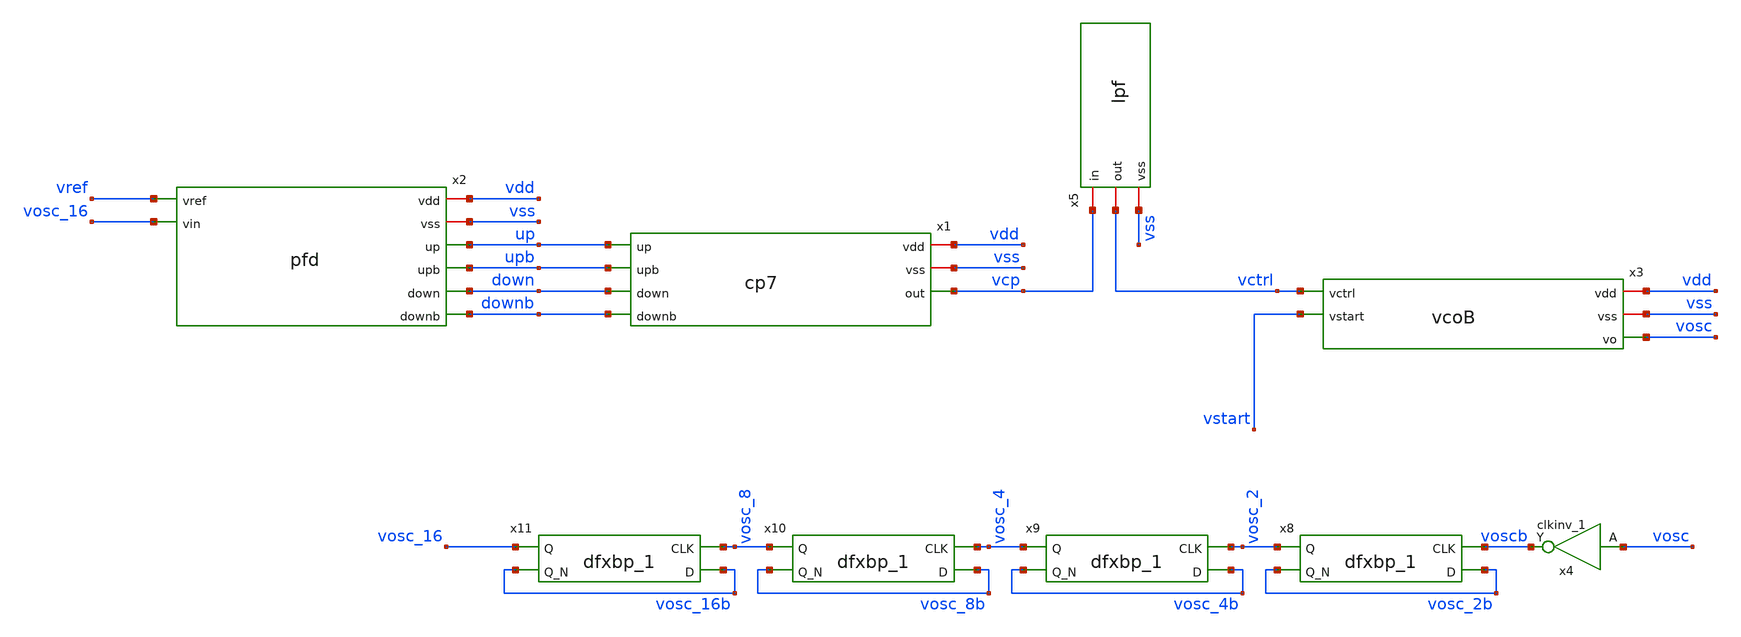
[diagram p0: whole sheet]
** sch_path: custom_gds/tt_um_mickey_pll/xschem/pll.sch
* custom_gds/tt_um_mickey_pll/xschem/inv_0p25.sym:
* Copyright 2022 Stefan Frederik Schippers
* Licensed under the Apache License, Version 2.0 (the "License");
.lib $::SKYWATER_MODELS/sky130.lib.spice tt
.include $::SKYWATER_STDCELLS/sky130_fd_sc_hd.spice

**.subckt pll
x1 vdd vss upb up vcp down downb cp7
x2 vdd vss vref up upb down vosc_16 downb pfd
x3 vdd vss vctrl vosc vstart vcoB
x8 voscb vosc_2b vss vss vdd vdd vosc_2 vosc_2b sky130_fd_sc_hd__dfxbp_1
x9 vosc_2 vosc_4b vss vss vdd vdd vosc_4 vosc_4b sky130_fd_sc_hd__dfxbp_1
x10 vosc_4 vosc_8b vss vss vdd vdd vosc_8 vosc_8b sky130_fd_sc_hd__dfxbp_1
x11 vosc_8 vosc_16b vss vss vdd vdd vosc_16 vosc_16b sky130_fd_sc_hd__dfxbp_1
x4 vosc vss vss vdd vdd voscb sky130_fd_sc_hd__clkinv_1
x5 vcp vctrl vss lpf
**** begin user architecture code



.param VCC=1.8
.options savecurrents
vvss vss 0 dc 0
vvdd vdd 0 dc VCC
**** vvctrl vctrl 0 dc 0.9
****vvctrl vctrl 0 PWL(0 0.9 100p 0.9 1000n 1.5)
vvstart vstart 0 PWL(0 1.8 100p 1.8 200p 0.0) dc 0
****vvstarve2 vstarve2 0 dc 1.8
vvref vref 0 PULSE(0.0 1.8 0n 1n 1n 80n 160n) dc 0

.ic v(vctrl)=0.8 v(vref)=0 v(vosc)=0

**** .ic v(vo_0)=1.8 v(vo_12)=0.0

**** interactive sim
.control
  remzerovec
  save all
  tran 100p 50000n
  remzerovec
  write untitled.raw
.endc



**** end user architecture code
**.ends

* expanding   symbol:  cp7.sym # of pins=7
** sym_path: custom_gds/tt_um_mickey_pll/xschem/cp7.sym
** sch_path: custom_gds/tt_um_mickey_pll/xschem/cp7.sch
.subckt cp7 vdd vss upb up out down downb
*.ipin upb
*.ipin up
*.ipin down
*.ipin downb
*.opin out
*.iopin vdd
*.iopin vss
XM1 vnb2 vnb3 vss vss sky130_fd_pr__nfet_01v8 L=0.60 W=1.80 nf=1 ad='int((nf+1)/2) * W/nf * 0.29' as='int((nf+2)/2) * W/nf * 0.29'
+ pd='2*int((nf+1)/2) * (W/nf + 0.29)' ps='2*int((nf+2)/2) * (W/nf + 0.29)' nrd='0.29 / W' nrs='0.29 / W'
+ sa=0 sb=0 sd=0 mult=1 m=1
XM2 out vnb vnb2 vss sky130_fd_pr__nfet_01v8 L=0.60 W=1.80 nf=1 ad='int((nf+1)/2) * W/nf * 0.29' as='int((nf+2)/2) * W/nf * 0.29'
+ pd='2*int((nf+1)/2) * (W/nf + 0.29)' ps='2*int((nf+2)/2) * (W/nf + 0.29)' nrd='0.29 / W' nrs='0.29 / W'
+ sa=0 sb=0 sd=0 mult=1 m=1
XM3 vnb3 vnb net1 vss sky130_fd_pr__nfet_01v8 L=0.60 W=1.80 nf=1 ad='int((nf+1)/2) * W/nf * 0.29' as='int((nf+2)/2) * W/nf * 0.29'
+ pd='2*int((nf+1)/2) * (W/nf + 0.29)' ps='2*int((nf+2)/2) * (W/nf + 0.29)' nrd='0.29 / W' nrs='0.29 / W'
+ sa=0 sb=0 sd=0 mult=1 m=1
XM4 net1 vnb3 vss vss sky130_fd_pr__nfet_01v8 L=0.60 W=1.80 nf=1 ad='int((nf+1)/2) * W/nf * 0.29' as='int((nf+2)/2) * W/nf * 0.29'
+ pd='2*int((nf+1)/2) * (W/nf + 0.29)' ps='2*int((nf+2)/2) * (W/nf + 0.29)' nrd='0.29 / W' nrs='0.29 / W'
+ sa=0 sb=0 sd=0 mult=1 m=1
XM5 vpb2 upb vss vss sky130_fd_pr__nfet_01v8 L=0.15 W=0.45 nf=1 ad='int((nf+1)/2) * W/nf * 0.29' as='int((nf+2)/2) * W/nf * 0.29'
+ pd='2*int((nf+1)/2) * (W/nf + 0.29)' ps='2*int((nf+2)/2) * (W/nf + 0.29)' nrd='0.29 / W' nrs='0.29 / W'
+ sa=0 sb=0 sd=0 mult=1 m=1
XM8 out vpb vpb2 vdd sky130_fd_pr__pfet_01v8 L=0.60 W=1.80 nf=1 ad='int((nf+1)/2) * W/nf * 0.29' as='int((nf+2)/2) * W/nf * 0.29'
+ pd='2*int((nf+1)/2) * (W/nf + 0.29)' ps='2*int((nf+2)/2) * (W/nf + 0.29)' nrd='0.29 / W' nrs='0.29 / W'
+ sa=0 sb=0 sd=0 mult=1 m=1
XM6 vpb2 vpb3 vdd vdd sky130_fd_pr__pfet_01v8 L=0.60 W=1.80 nf=1 ad='int((nf+1)/2) * W/nf * 0.29' as='int((nf+2)/2) * W/nf * 0.29'
+ pd='2*int((nf+1)/2) * (W/nf + 0.29)' ps='2*int((nf+2)/2) * (W/nf + 0.29)' nrd='0.29 / W' nrs='0.29 / W'
+ sa=0 sb=0 sd=0 mult=1 m=1
XM7 vpb3 vpb net2 vdd sky130_fd_pr__pfet_01v8 L=0.60 W=1.80 nf=1 ad='int((nf+1)/2) * W/nf * 0.29' as='int((nf+2)/2) * W/nf * 0.29'
+ pd='2*int((nf+1)/2) * (W/nf + 0.29)' ps='2*int((nf+2)/2) * (W/nf + 0.29)' nrd='0.29 / W' nrs='0.29 / W'
+ sa=0 sb=0 sd=0 mult=1 m=1
XM9 net2 vpb3 vdd vdd sky130_fd_pr__pfet_01v8 L=0.60 W=1.80 nf=1 ad='int((nf+1)/2) * W/nf * 0.29' as='int((nf+2)/2) * W/nf * 0.29'
+ pd='2*int((nf+1)/2) * (W/nf + 0.29)' ps='2*int((nf+2)/2) * (W/nf + 0.29)' nrd='0.29 / W' nrs='0.29 / W'
+ sa=0 sb=0 sd=0 mult=1 m=1
XM10 vnb2 down vdd vdd sky130_fd_pr__pfet_01v8 L=0.15 W=0.60 nf=1 ad='int((nf+1)/2) * W/nf * 0.29' as='int((nf+2)/2) * W/nf * 0.29'
+ pd='2*int((nf+1)/2) * (W/nf + 0.29)' ps='2*int((nf+2)/2) * (W/nf + 0.29)' nrd='0.29 / W' nrs='0.29 / W'
+ sa=0 sb=0 sd=0 mult=1 m=1
XM11 vnb vnb vss vss sky130_fd_pr__nfet_01v8 L=0.60 W=0.45 nf=1 ad='int((nf+1)/2) * W/nf * 0.29' as='int((nf+2)/2) * W/nf * 0.29'
+ pd='2*int((nf+1)/2) * (W/nf + 0.29)' ps='2*int((nf+2)/2) * (W/nf + 0.29)' nrd='0.29 / W' nrs='0.29 / W'
+ sa=0 sb=0 sd=0 mult=1 m=1
XM12 vpb vpb vdd vdd sky130_fd_pr__pfet_01v8 L=0.60 W=0.45 nf=1 ad='int((nf+1)/2) * W/nf * 0.29' as='int((nf+2)/2) * W/nf * 0.29'
+ pd='2*int((nf+1)/2) * (W/nf + 0.29)' ps='2*int((nf+2)/2) * (W/nf + 0.29)' nrd='0.29 / W' nrs='0.29 / W'
+ sa=0 sb=0 sd=0 mult=1 m=1
x2 vdd G_vnb G_vpb vss bias
XM13 vnb G_vpb vdd vdd sky130_fd_pr__pfet_01v8 L=0.60 W=1.80 nf=1 ad='int((nf+1)/2) * W/nf * 0.29' as='int((nf+2)/2) * W/nf * 0.29'
+ pd='2*int((nf+1)/2) * (W/nf + 0.29)' ps='2*int((nf+2)/2) * (W/nf + 0.29)' nrd='0.29 / W' nrs='0.29 / W'
+ sa=0 sb=0 sd=0 mult=1 m=1
XM14 vpb G_vnb vss vss sky130_fd_pr__nfet_01v8 L=0.60 W=1.80 nf=1 ad='int((nf+1)/2) * W/nf * 0.29' as='int((nf+2)/2) * W/nf * 0.29'
+ pd='2*int((nf+1)/2) * (W/nf + 0.29)' ps='2*int((nf+2)/2) * (W/nf + 0.29)' nrd='0.29 / W' nrs='0.29 / W'
+ sa=0 sb=0 sd=0 mult=1 m=1
XM15 vpb3 G_vnb vss vss sky130_fd_pr__nfet_01v8 L=0.60 W=1.80 nf=1 ad='int((nf+1)/2) * W/nf * 0.29' as='int((nf+2)/2) * W/nf * 0.29'
+ pd='2*int((nf+1)/2) * (W/nf + 0.29)' ps='2*int((nf+2)/2) * (W/nf + 0.29)' nrd='0.29 / W' nrs='0.29 / W'
+ sa=0 sb=0 sd=0 mult=1 m=1
XM16 vnb3 G_vpb vdd vdd sky130_fd_pr__pfet_01v8 L=0.60 W=1.80 nf=1 ad='int((nf+1)/2) * W/nf * 0.29' as='int((nf+2)/2) * W/nf * 0.29'
+ pd='2*int((nf+1)/2) * (W/nf + 0.29)' ps='2*int((nf+2)/2) * (W/nf + 0.29)' nrd='0.29 / W' nrs='0.29 / W'
+ sa=0 sb=0 sd=0 mult=1 m=1
.ends


* expanding   symbol:  pfd.sym # of pins=8
** sym_path: custom_gds/tt_um_mickey_pll/xschem/pfd.sym
** sch_path: custom_gds/tt_um_mickey_pll/xschem/pfd.sch
.subckt pfd vdd vss vref up upb down vin downb
*.ipin vref
*.ipin vin
*.iopin vdd
*.iopin vss
*.opin up
*.opin down
*.opin downb
*.opin upb
x1 vref vdd rstb vss vss vdd vdd net1 upb sky130_fd_sc_hd__dfrbp_1
x2 vin vdd rstb vss vss vdd vdd net2 downb sky130_fd_sc_hd__dfrbp_1
x3 net1 vss vss vdd vdd up sky130_fd_sc_hd__buf_8
x4 net2 vss vss vdd vdd down sky130_fd_sc_hd__buf_8
x5 up down vss vss vdd vdd rstb sky130_fd_sc_hd__nand2_1
.ends


* expanding   symbol:  vcoB.sym # of pins=5
** sym_path: custom_gds/tt_um_mickey_pll/xschem/vcoB.sym
** sch_path: custom_gds/tt_um_mickey_pll/xschem/vcoB.sch
.subckt vcoB vdd vss vctrl vo vstart
*.ipin vctrl
*.iopin vdd
*.iopin vss
*.ipin vstart
*.opin vo
XM1 vpb vctrl vss vss sky130_fd_pr__nfet_01v8 L=0.6 W=0.5 nf=1 ad='int((nf+1)/2) * W/nf * 0.29' as='int((nf+2)/2) * W/nf * 0.29'
+ pd='2*int((nf+1)/2) * (W/nf + 0.29)' ps='2*int((nf+2)/2) * (W/nf + 0.29)' nrd='0.29 / W' nrs='0.29 / W'
+ sa=0 sb=0 sd=0 mult=1 m=1
XM2 vpb vpb vdd vdd sky130_fd_pr__pfet_01v8 L=0.15 W=2.0 nf=4 ad='int((nf+1)/2) * W/nf * 0.29' as='int((nf+2)/2) * W/nf * 0.29'
+ pd='2*int((nf+1)/2) * (W/nf + 0.29)' ps='2*int((nf+2)/2) * (W/nf + 0.29)' nrd='0.29 / W' nrs='0.29 / W'
+ sa=0 sb=0 sd=0 mult=1 m=1
x13 vo_5 vo_12 vstarve vss inv_0p25
XM3 vstarve vpb vdd vdd sky130_fd_pr__pfet_01v8 L=0.15 W=2.0 nf=4 ad='int((nf+1)/2) * W/nf * 0.29' as='int((nf+2)/2) * W/nf * 0.29'
+ pd='2*int((nf+1)/2) * (W/nf + 0.29)' ps='2*int((nf+2)/2) * (W/nf + 0.29)' nrd='0.29 / W' nrs='0.29 / W'
+ sa=0 sb=0 sd=0 mult=1 m=1
XM4 vo_0 vstart vss vss sky130_fd_pr__nfet_01v8 L=0.15 W=3.0 nf=6 ad='int((nf+1)/2) * W/nf * 0.29' as='int((nf+2)/2) * W/nf * 0.29'
+ pd='2*int((nf+1)/2) * (W/nf + 0.29)' ps='2*int((nf+2)/2) * (W/nf + 0.29)' nrd='0.29 / W' nrs='0.29 / W'
+ sa=0 sb=0 sd=0 mult=1 m=1
x12 vo_12 vo_0 vstarve vss inv_0p25
x1 vo_0 vo_1 vstarve vss inv_0p25
x2 vo_1 vo_2 vstarve vss inv_0p25
x3 vo_2 vo_3 vstarve vss inv_0p25
x4 vo_3 vo_4 vstarve vss inv_0p25
x5 vo_4 vo_5 vstarve vss inv_0p25
x6 vo_12 vss vss vdd vdd vo sky130_fd_sc_hd__inv_1
XR3 vstarve vdd vss sky130_fd_pr__res_xhigh_po W=0.35 L=17.5 mult=1 m=1
.ends


* expanding   symbol:  lpf.sym # of pins=3
** sym_path: custom_gds/tt_um_mickey_pll/xschem/lpf.sym
** sch_path: custom_gds/tt_um_mickey_pll/xschem/lpf.sch
.subckt lpf in out vss
*.iopin in
*.iopin vss
*.iopin out
R2 out in 0.1 m=1
XR1 net1 in vss sky130_fd_pr__res_high_po W=0.690 L=20.35 mult=1 m=1
XC1 vss in sky130_fd_pr__cap_mim_m3_1 W=22.175 L=22.175 MF=1 m=1
XC2 vss net1 sky130_fd_pr__cap_mim_m3_1 W=22.175 L=22.175 MF=5 m=5
.ends


* expanding   symbol:  bias.sym # of pins=4
** sym_path: custom_gds/tt_um_mickey_pll/xschem/bias.sym
** sch_path: custom_gds/tt_um_mickey_pll/xschem/bias.sch
.subckt bias vdd vnb vpb vss
*.iopin vdd
*.iopin vss
*.iopin vnb
*.iopin vpb
XM1 vpb vnb vss vss sky130_fd_pr__nfet_01v8 L=0.60 W=1.80 nf=1 ad='int((nf+1)/2) * W/nf * 0.29' as='int((nf+2)/2) * W/nf * 0.29'
+ pd='2*int((nf+1)/2) * (W/nf + 0.29)' ps='2*int((nf+2)/2) * (W/nf + 0.29)' nrd='0.29 / W' nrs='0.29 / W'
+ sa=0 sb=0 sd=0 mult=1 m=1
XM2 vnb vnb vss vss sky130_fd_pr__nfet_01v8 L=0.60 W=1.80 nf=1 ad='int((nf+1)/2) * W/nf * 0.29' as='int((nf+2)/2) * W/nf * 0.29'
+ pd='2*int((nf+1)/2) * (W/nf + 0.29)' ps='2*int((nf+2)/2) * (W/nf + 0.29)' nrd='0.29 / W' nrs='0.29 / W'
+ sa=0 sb=0 sd=0 mult=1 m=1
XM3 vpb vpb vdd vdd sky130_fd_pr__pfet_01v8 L=0.60 W=1.80 nf=1 ad='int((nf+1)/2) * W/nf * 0.29' as='int((nf+2)/2) * W/nf * 0.29'
+ pd='2*int((nf+1)/2) * (W/nf + 0.29)' ps='2*int((nf+2)/2) * (W/nf + 0.29)' nrd='0.29 / W' nrs='0.29 / W'
+ sa=0 sb=0 sd=0 mult=1 m=1
XM4 vnb vpb net1 vdd sky130_fd_pr__pfet_01v8 L=0.60 W=7.20 nf=4 ad='int((nf+1)/2) * W/nf * 0.29' as='int((nf+2)/2) * W/nf * 0.29'
+ pd='2*int((nf+1)/2) * (W/nf + 0.29)' ps='2*int((nf+2)/2) * (W/nf + 0.29)' nrd='0.29 / W' nrs='0.29 / W'
+ sa=0 sb=0 sd=0 mult=1 m=1
XM5 net2 vpb vdd vdd sky130_fd_pr__pfet_01v8 L=0.60 W=1.80 nf=1 ad='int((nf+1)/2) * W/nf * 0.29' as='int((nf+2)/2) * W/nf * 0.29'
+ pd='2*int((nf+1)/2) * (W/nf + 0.29)' ps='2*int((nf+2)/2) * (W/nf + 0.29)' nrd='0.29 / W' nrs='0.29 / W'
+ sa=0 sb=0 sd=0 mult=1 m=1
XM6 net2 net2 vss vss sky130_fd_pr__nfet_01v8 L=1.50 W=0.45 nf=1 ad='int((nf+1)/2) * W/nf * 0.29' as='int((nf+2)/2) * W/nf * 0.29'
+ pd='2*int((nf+1)/2) * (W/nf + 0.29)' ps='2*int((nf+2)/2) * (W/nf + 0.29)' nrd='0.29 / W' nrs='0.29 / W'
+ sa=0 sb=0 sd=0 mult=1 m=1
XM7 vnb net2 vpb vdd sky130_fd_pr__pfet_01v8 L=0.60 W=0.9 nf=1 ad='int((nf+1)/2) * W/nf * 0.29' as='int((nf+2)/2) * W/nf * 0.29'
+ pd='2*int((nf+1)/2) * (W/nf + 0.29)' ps='2*int((nf+2)/2) * (W/nf + 0.29)' nrd='0.29 / W' nrs='0.29 / W'
+ sa=0 sb=0 sd=0 mult=1 m=1
XR1 net1 vdd vdd sky130_fd_pr__res_xhigh_po_0p35 L=2.000 mult=1 m=1
.ends


* expanding   symbol:  sky130_stdcells/inv_0p25.sym # of pins=5
** sym_path: custom_gds/tt_um_mickey_pll/xschem/inv_0p25.sym
** sch_path: custom_gds/tt_um_mickey_pll/xschem/inv_0p25.sch
.subckt inv_0p25 A Y VDD VSS
*.ipin A
*.iopin VDD
*.iopin VSS
*.opin Y
XM1 Y A VSS VSS sky130_fd_pr__nfet_01v8 L=0.60 W=0.65 nf=1 ad='int((nf+1)/2) * W/nf * 0.29' as='int((nf+2)/2) * W/nf * 0.29'
+ pd='2*int((nf+1)/2) * (W/nf + 0.29)' ps='2*int((nf+2)/2) * (W/nf + 0.29)' nrd='0.29 / W' nrs='0.29 / W'
+ sa=0 sb=0 sd=0 mult=1 m=1
XM2 Y A VDD VDD sky130_fd_pr__pfet_01v8_hvt L=0.60 W=1 nf=1 ad='int((nf+1)/2) * W/nf * 0.29' as='int((nf+2)/2) * W/nf * 0.29'
+ pd='2*int((nf+1)/2) * (W/nf + 0.29)' ps='2*int((nf+2)/2) * (W/nf + 0.29)' nrd='0.29 / W' nrs='0.29 / W'
+ sa=0 sb=0 sd=0 mult=1 m=1
.ends

.end
